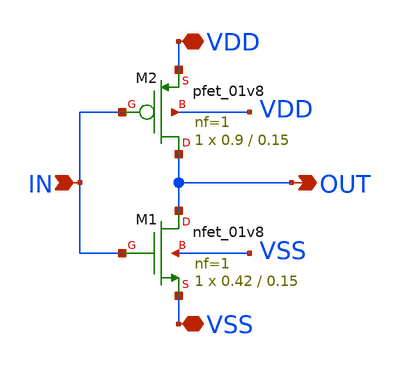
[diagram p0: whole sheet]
** sch_path: design/ALU/inverter.sch
**.subckt inverter IN VDD OUT VSS
*.ipin IN
*.iopin VDD
*.opin OUT
*.iopin VSS
XM2 OUT IN VDD VDD sky130_fd_pr__pfet_01v8 L=0.15 W=0.9 nf=1 ad='int((nf+1)/2) * W/nf * 0.29' as='int((nf+2)/2) * W/nf * 0.29'
+ pd='2*int((nf+1)/2) * (W/nf + 0.29)' ps='2*int((nf+2)/2) * (W/nf + 0.29)' nrd='0.29 / W' nrs='0.29 / W'
+ sa=0 sb=0 sd=0 mult=1 m=1
XM1 OUT IN VSS VSS sky130_fd_pr__nfet_01v8 L=0.15 W=0.42 nf=1 ad='int((1 + 1)/2) * 0.42 / 1 * 0.29' as='int((1 + 2)/2) * 0.42 / 1 * 0.29'
+ pd='2*int((1 + 1)/2) * (0.42 / 1 + 0.29)' ps='2*int((1 + 2)/2) * (0.42 / 1 + 0.29)' nrd='0.29 / 0.42 '
+ nrs='0.29 / 0.42 ' sa=0 sb=0 sd=0 mult=1 m=1
**.ends
.end
